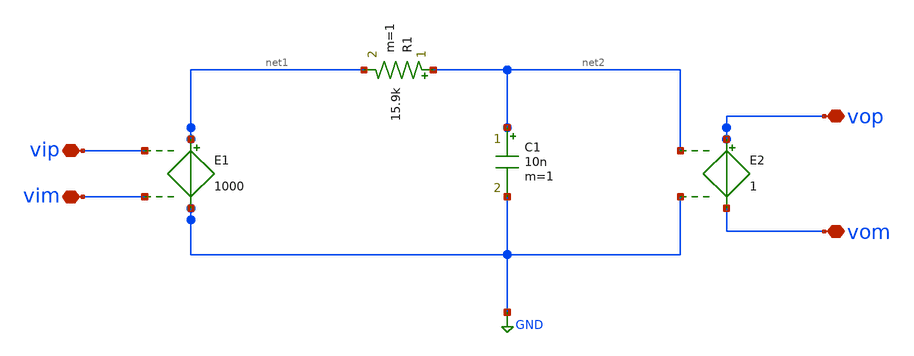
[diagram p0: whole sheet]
** sch_path: xschem/untitled-1.sch
**.subckt untitled-1 vip vim vop vom
*.iopin vip
*.iopin vim
*.iopin vop
*.iopin vom
E1 net1 GND vip vim 1000
E2 vop vom net2 GND 1
R1 net2 net1 15.9k m=1
C1 net2 GND 10n m=1
**.ends
.GLOBAL GND
.end
